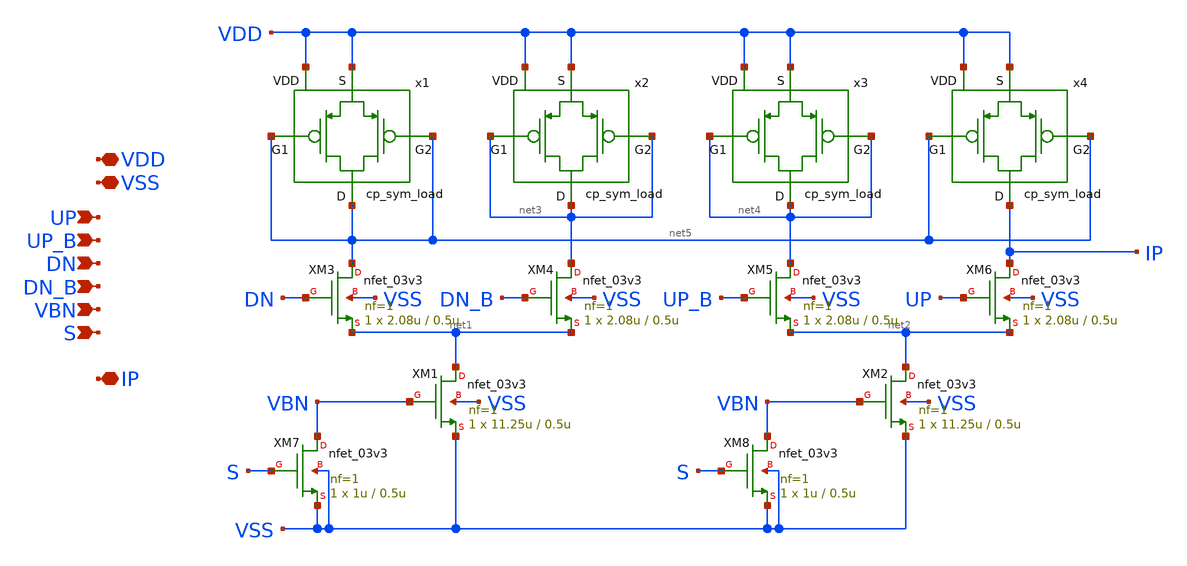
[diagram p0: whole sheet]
** sch_path: designs/libs/core_analog/charge_pump/charge_pump.sch
**.subckt charge_pump VDD VSS UP UP_B DN DN_B VBN IP S
*.iopin VDD
*.iopin VSS
*.ipin UP
*.ipin UP_B
*.ipin DN
*.ipin DN_B
*.ipin VBN
*.iopin IP
*.ipin S
x1 net5 net5 VDD net5 VDD cp_sym_load
x2 net3 net3 VDD net3 VDD cp_sym_load
x3 net4 net4 VDD net4 VDD cp_sym_load
x4 net5 net5 VDD IP VDD cp_sym_load
XM1 net1 VBN VSS VSS nfet_03v3 L=0.5u W=11.25u nf=1 ad='int((nf+1)/2) * W/nf * 0.18u' as='int((nf+2)/2) * W/nf * 0.18u'
+ pd='2*int((nf+1)/2) * (W/nf + 0.18u)' ps='2*int((nf+2)/2) * (W/nf + 0.18u)' nrd='0.18u / W' nrs='0.18u / W'
+ sa=0 sb=0 sd=0 m=1
XM3 net5 DN net1 VSS nfet_03v3 L=0.5u W=2.08u nf=1 ad='int((nf+1)/2) * W/nf * 0.18u' as='int((nf+2)/2) * W/nf * 0.18u'
+ pd='2*int((nf+1)/2) * (W/nf + 0.18u)' ps='2*int((nf+2)/2) * (W/nf + 0.18u)' nrd='0.18u / W' nrs='0.18u / W'
+ sa=0 sb=0 sd=0 m=1
XM7 VBN S VSS VSS nfet_03v3 L=0.5u W=1u nf=1 ad='int((nf+1)/2) * W/nf * 0.18u' as='int((nf+2)/2) * W/nf * 0.18u'
+ pd='2*int((nf+1)/2) * (W/nf + 0.18u)' ps='2*int((nf+2)/2) * (W/nf + 0.18u)' nrd='0.18u / W' nrs='0.18u / W'
+ sa=0 sb=0 sd=0 m=1
XM8 VBN S VSS VSS nfet_03v3 L=0.5u W=1u nf=1 ad='int((nf+1)/2) * W/nf * 0.18u' as='int((nf+2)/2) * W/nf * 0.18u'
+ pd='2*int((nf+1)/2) * (W/nf + 0.18u)' ps='2*int((nf+2)/2) * (W/nf + 0.18u)' nrd='0.18u / W' nrs='0.18u / W'
+ sa=0 sb=0 sd=0 m=1
XM4 net3 DN_B net1 VSS nfet_03v3 L=0.5u W=2.08u nf=1 ad='int((nf+1)/2) * W/nf * 0.18u' as='int((nf+2)/2) * W/nf * 0.18u'
+ pd='2*int((nf+1)/2) * (W/nf + 0.18u)' ps='2*int((nf+2)/2) * (W/nf + 0.18u)' nrd='0.18u / W' nrs='0.18u / W'
+ sa=0 sb=0 sd=0 m=1
XM5 net4 UP_B net2 VSS nfet_03v3 L=0.5u W=2.08u nf=1 ad='int((nf+1)/2) * W/nf * 0.18u' as='int((nf+2)/2) * W/nf * 0.18u'
+ pd='2*int((nf+1)/2) * (W/nf + 0.18u)' ps='2*int((nf+2)/2) * (W/nf + 0.18u)' nrd='0.18u / W' nrs='0.18u / W'
+ sa=0 sb=0 sd=0 m=1
XM6 IP UP net2 VSS nfet_03v3 L=0.5u W=2.08u nf=1 ad='int((nf+1)/2) * W/nf * 0.18u' as='int((nf+2)/2) * W/nf * 0.18u'
+ pd='2*int((nf+1)/2) * (W/nf + 0.18u)' ps='2*int((nf+2)/2) * (W/nf + 0.18u)' nrd='0.18u / W' nrs='0.18u / W'
+ sa=0 sb=0 sd=0 m=1
XM2 net2 VBN VSS VSS nfet_03v3 L=0.5u W=11.25u nf=1 ad='int((nf+1)/2) * W/nf * 0.18u' as='int((nf+2)/2) * W/nf * 0.18u'
+ pd='2*int((nf+1)/2) * (W/nf + 0.18u)' ps='2*int((nf+2)/2) * (W/nf + 0.18u)' nrd='0.18u / W' nrs='0.18u / W'
+ sa=0 sb=0 sd=0 m=1
**.ends

* expanding   symbol:  libs/core_analog/cp_sym_load/cp_sym_load.sym # of pins=5
** sym_path: designs/libs/core_analog/cp_sym_load/cp_sym_load.sym
** sch_path: designs/libs/core_analog/cp_sym_load/cp_sym_load.sch
.subckt cp_sym_load G1 G2 S D VDD
*.ipin G1
*.ipin G2
*.iopin S
*.iopin D
*.iopin VDD
XM1 D G1 S VDD pfet_03v3 L=1.5u W=1.1u nf=1 ad='int((nf+1)/2) * W/nf * 0.18u' as='int((nf+2)/2) * W/nf * 0.18u'
+ pd='2*int((nf+1)/2) * (W/nf + 0.18u)' ps='2*int((nf+2)/2) * (W/nf + 0.18u)' nrd='0.18u / W' nrs='0.18u / W'
+ sa=0 sb=0 sd=0 m=1
XM2 D G2 S VDD pfet_03v3 L=1.5u W=1.1u nf=1 ad='int((nf+1)/2) * W/nf * 0.18u' as='int((nf+2)/2) * W/nf * 0.18u'
+ pd='2*int((nf+1)/2) * (W/nf + 0.18u)' ps='2*int((nf+2)/2) * (W/nf + 0.18u)' nrd='0.18u / W' nrs='0.18u / W'
+ sa=0 sb=0 sd=0 m=1
.ends

.end
